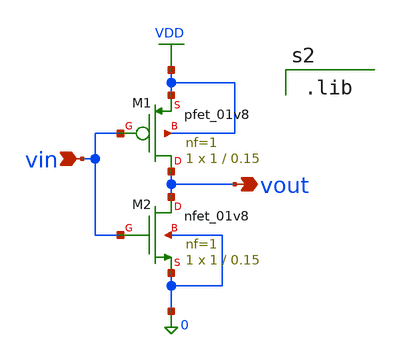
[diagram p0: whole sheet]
** sch_path: Lab2-Xschem-CMOS/inverter.sch
**.subckt inverter vin vout
*.ipin vin
*.opin vout
XM1 vout vin VDD VDD sky130_fd_pr__pfet_01v8 L=0.15 W=1 nf=1 ad='int((1 + 1)/2) * 1 / 1 * 0.29' as='int((1 + 2)/2) * 1 / 1 * 0.29'
+ pd='2*int((1 + 1)/2) * (1 / 1 + 0.29)' ps='2*int((1 + 2)/2) * (1 / 1 + 0.29)' nrd='0.29 / 1 ' nrs='0.29 / 1 '
+ sa=0 sb=0 sd=0 mult=1 m=1
XM2 vout vin 0 0 sky130_fd_pr__nfet_01v8 L=0.15 W=1 nf=1 ad='int((1 + 1)/2) * 1 / 1 * 0.29' as='int((1 + 2)/2) * 1 / 1 * 0.29'
+ pd='2*int((1 + 1)/2) * (1 / 1 + 0.29)' ps='2*int((1 + 2)/2) * (1 / 1 + 0.29)' nrd='0.29 / 1 ' nrs='0.29 / 1 '
+ sa=0 sb=0 sd=0 mult=1 m=1
**** begin user architecture code


V_VDD VDD 0 1.8
V_VIN vin 0 0
.control
 dc V_VIN 0 1.8 0.01
 plot v(vout) v(vin)
.endc


.lib

**** end user architecture code
**.ends
.GLOBAL VDD
.end
